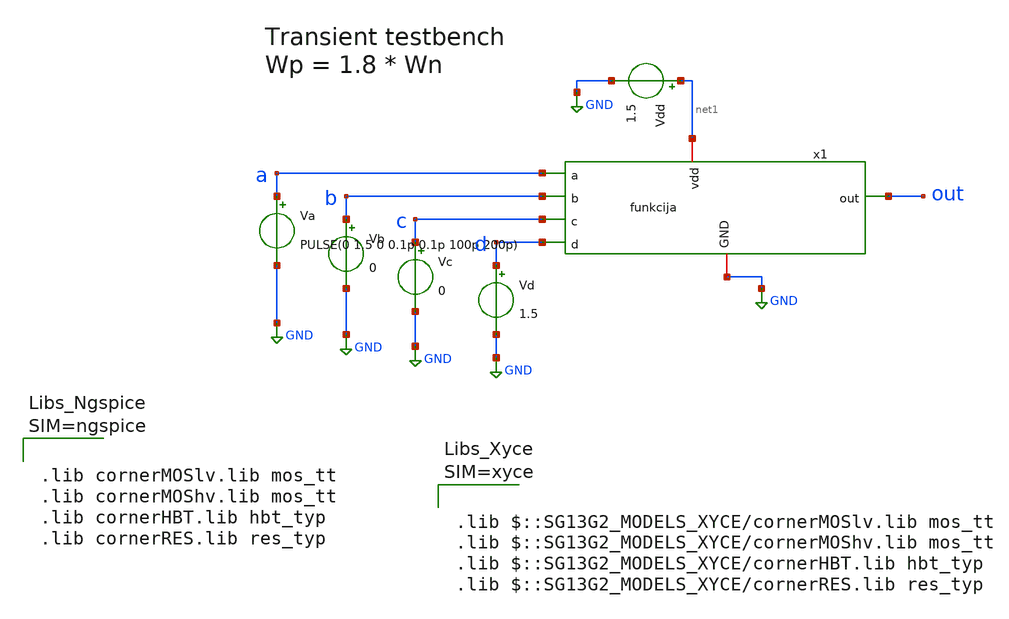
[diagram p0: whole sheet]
** sch_path: projekat/slucaj_1_8/testbench/tb_tran.sch
**.subckt tb_tran
Va a GND PULSE(0 1.5 0 0.1p 0.1p 100p 200p)
Vb b GND 0
Vc c GND 0
Vd d GND 1.5
Vdd net1 GND 1.5
x1 net1 out d a c b GND funkcija
**** begin user architecture code



.lib cornerMOSlv.lib mos_tt
.lib cornerMOShv.lib mos_tt
.lib cornerHBT.lib hbt_typ
.lib cornerRES.lib res_typ









.tran 0.1p 500p

.control
  save all
  run

  meas tran tr_out TRIG v(out) VAL=0.15 RISE=2 TARG v(out) VAL=1.35 RISE=2
  meas tran tf_out TRIG v(out) VAL=1.35 FALL=2 TARG v(out) VAL=0.15 FALL=2

  plot v(a)+6 v(b)+4.5 v(c)+3 v(d)+1.5 v(out)
  print tr_out tf_out
  wrdata /home/Nikola.Jankovic/projekat/slucaj_1_8/python/odziv_1_8.txt v(a) v(out)
.endc

**** end user architecture code
**.ends

* expanding   symbol:  /home/Nikola.Jankovic/projekat/slucaj_1_8/schematic/funkcija.sym # of pins=7
** sym_path: projekat/slucaj_2/schematic/funkcija.sym
** sch_path: projekat/slucaj_2/schematic/funkcija.sch
.subckt funkcija vdd out d a c b GND
*.ipin a
*.ipin b
*.ipin c
*.ipin d
*.iopin vdd
*.iopin GND
*.opin out
XM1 net1 a GND GND sg13_lv_nmos w=0.3u l=0.13u ng=1 m=1 mm_ok=1
XM2 net1 b GND GND sg13_lv_nmos w=0.3u l=0.13u ng=1 m=1 mm_ok=1
XM3 net1 c GND GND sg13_lv_nmos w=0.3u l=0.13u ng=1 m=1 mm_ok=1
XM4 out d net1 GND sg13_lv_nmos w=0.3u l=0.13u ng=1 m=1 mm_ok=1
XM5 net2 a vdd vdd sg13_lv_pmos w=0.9u l=0.13u ng=1 m=1 mm_ok=1
XM6 net3 b net2 vdd sg13_lv_pmos w=0.9u l=0.13u ng=1 m=1 mm_ok=1
XM7 out c net3 vdd sg13_lv_pmos w=0.9u l=0.13u ng=1 m=1 mm_ok=1
XM8 out d vdd vdd sg13_lv_pmos w=0.3u l=0.13u ng=1 m=1 mm_ok=1
.ends

.GLOBAL GND
.end
